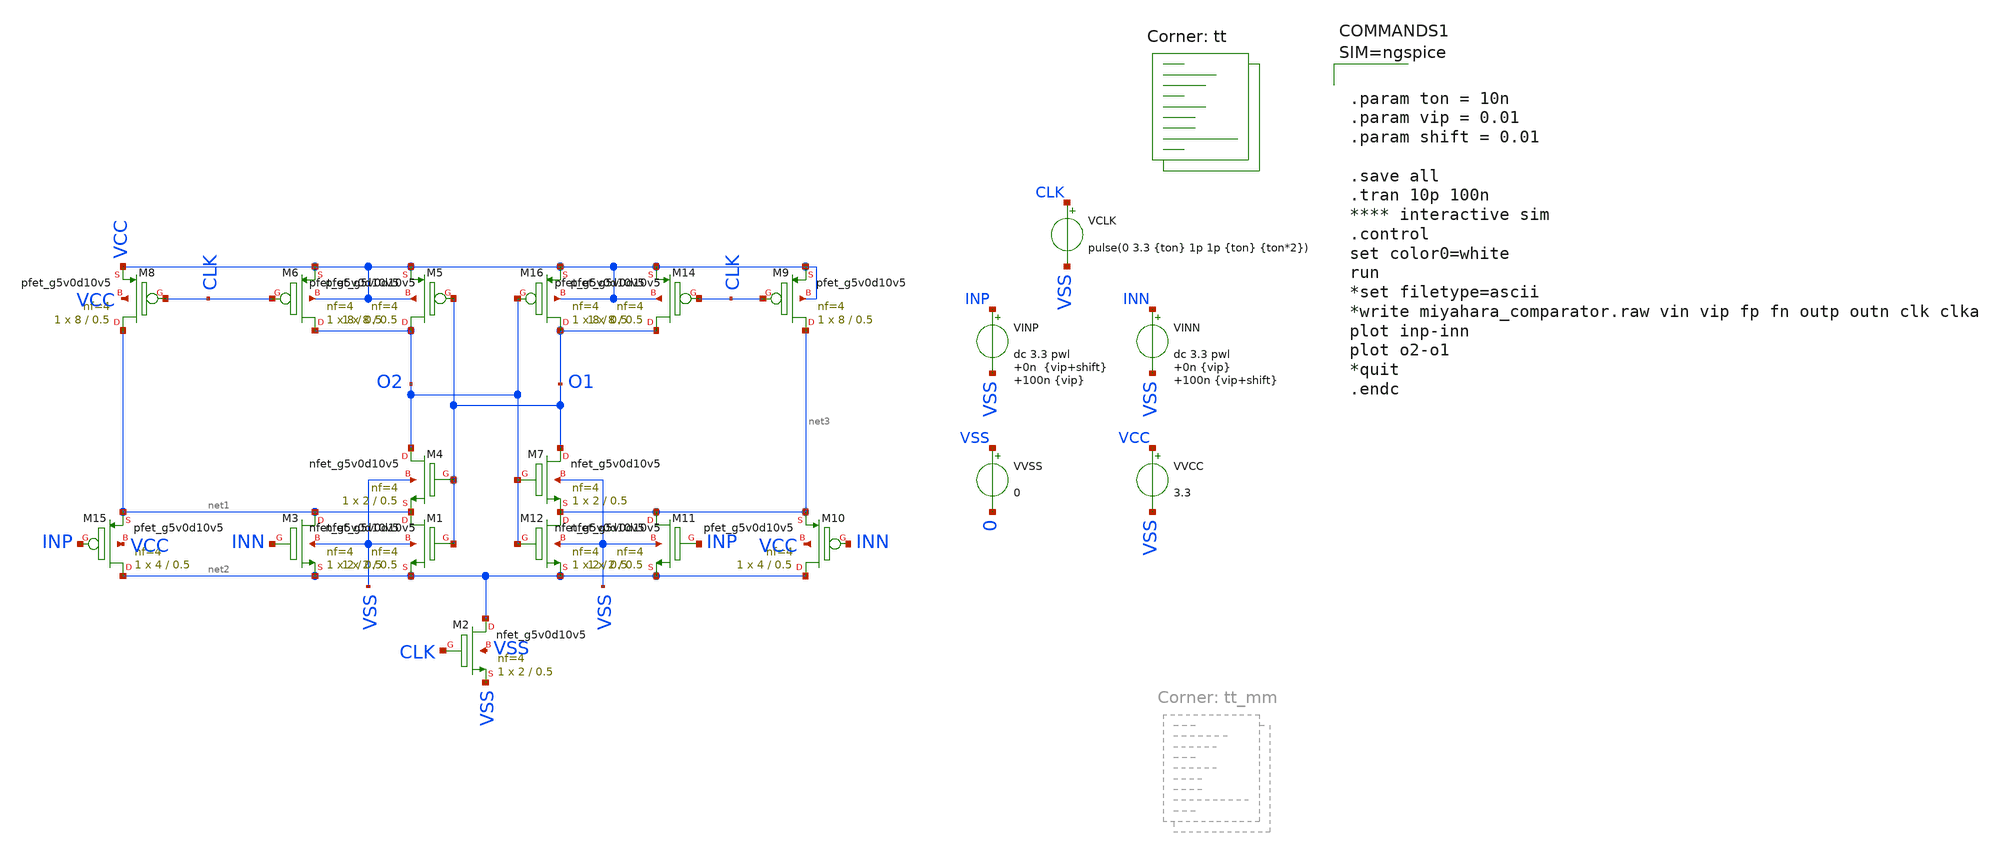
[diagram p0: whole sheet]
** sch_path: Comparator/schematic/new_comparator/comparator_rail2rail_working.sch
**.subckt comparator_rail2rail_working
VINP INP VSS dc 3.3 pwl 0n {vip+shift} 100n {vip}
VINN INN VSS dc 3.3 pwl 0n {vip} 100n {vip+shift}
XM15 net2 INP net1 VCC sky130_fd_pr__pfet_g5v0d10v5 L=0.5 W=4 nf=4 ad='int((nf+1)/2) * W/nf * 0.29' as='int((nf+2)/2) * W/nf * 0.29'
+ pd='2*int((nf+1)/2) * (W/nf + 0.29)' ps='2*int((nf+2)/2) * (W/nf + 0.29)' nrd='0.29 / W' nrs='0.29 / W'
+ sa=0 sb=0 sd=0 mult=1 m=1
XM2 net2 CLK VSS VSS sky130_fd_pr__nfet_g5v0d10v5 L=0.5 W=2 nf=4 ad='int((nf+1)/2) * W/nf * 0.29' as='int((nf+2)/2) * W/nf * 0.29'
+ pd='2*int((nf+1)/2) * (W/nf + 0.29)' ps='2*int((nf+2)/2) * (W/nf + 0.29)' nrd='0.29 / W' nrs='0.29 / W'
+ sa=0 sb=0 sd=0 mult=1 m=1
XM8 net1 CLK VCC VCC sky130_fd_pr__pfet_g5v0d10v5 L=0.5 W=8 nf=4 ad='int((nf+1)/2) * W/nf * 0.29' as='int((nf+2)/2) * W/nf * 0.29'
+ pd='2*int((nf+1)/2) * (W/nf + 0.29)' ps='2*int((nf+2)/2) * (W/nf + 0.29)' nrd='0.29 / W' nrs='0.29 / W'
+ sa=0 sb=0 sd=0 mult=1 m=1
XM1 net1 O1 net2 VSS sky130_fd_pr__nfet_g5v0d10v5 L=0.5 W=2 nf=4 ad='int((nf+1)/2) * W/nf * 0.29' as='int((nf+2)/2) * W/nf * 0.29'
+ pd='2*int((nf+1)/2) * (W/nf + 0.29)' ps='2*int((nf+2)/2) * (W/nf + 0.29)' nrd='0.29 / W' nrs='0.29 / W'
+ sa=0 sb=0 sd=0 mult=1 m=1
XM3 net1 INN net2 VSS sky130_fd_pr__nfet_g5v0d10v5 L=0.5 W=2 nf=4 ad='int((nf+1)/2) * W/nf * 0.29' as='int((nf+2)/2) * W/nf * 0.29'
+ pd='2*int((nf+1)/2) * (W/nf + 0.29)' ps='2*int((nf+2)/2) * (W/nf + 0.29)' nrd='0.29 / W' nrs='0.29 / W'
+ sa=0 sb=0 sd=0 mult=1 m=1
XM4 O2 O1 net1 VSS sky130_fd_pr__nfet_g5v0d10v5 L=0.5 W=2 nf=4 ad='int((nf+1)/2) * W/nf * 0.29' as='int((nf+2)/2) * W/nf * 0.29'
+ pd='2*int((nf+1)/2) * (W/nf + 0.29)' ps='2*int((nf+2)/2) * (W/nf + 0.29)' nrd='0.29 / W' nrs='0.29 / W'
+ sa=0 sb=0 sd=0 mult=1 m=1
XM5 O2 O1 VCC VCC sky130_fd_pr__pfet_g5v0d10v5 L=0.5 W=8 nf=4 ad='int((nf+1)/2) * W/nf * 0.29' as='int((nf+2)/2) * W/nf * 0.29'
+ pd='2*int((nf+1)/2) * (W/nf + 0.29)' ps='2*int((nf+2)/2) * (W/nf + 0.29)' nrd='0.29 / W' nrs='0.29 / W'
+ sa=0 sb=0 sd=0 mult=1 m=1
XM6 O2 CLK VCC VCC sky130_fd_pr__pfet_g5v0d10v5 L=0.5 W=8 nf=4 ad='int((nf+1)/2) * W/nf * 0.29' as='int((nf+2)/2) * W/nf * 0.29'
+ pd='2*int((nf+1)/2) * (W/nf + 0.29)' ps='2*int((nf+2)/2) * (W/nf + 0.29)' nrd='0.29 / W' nrs='0.29 / W'
+ sa=0 sb=0 sd=0 mult=1 m=1
XM11 net3 INP net2 VSS sky130_fd_pr__nfet_g5v0d10v5 L=0.5 W=2 nf=4 ad='int((nf+1)/2) * W/nf * 0.29' as='int((nf+2)/2) * W/nf * 0.29'
+ pd='2*int((nf+1)/2) * (W/nf + 0.29)' ps='2*int((nf+2)/2) * (W/nf + 0.29)' nrd='0.29 / W' nrs='0.29 / W'
+ sa=0 sb=0 sd=0 mult=1 m=1
XM12 net3 O2 net2 VSS sky130_fd_pr__nfet_g5v0d10v5 L=0.5 W=2 nf=4 ad='int((nf+1)/2) * W/nf * 0.29' as='int((nf+2)/2) * W/nf * 0.29'
+ pd='2*int((nf+1)/2) * (W/nf + 0.29)' ps='2*int((nf+2)/2) * (W/nf + 0.29)' nrd='0.29 / W' nrs='0.29 / W'
+ sa=0 sb=0 sd=0 mult=1 m=1
XM14 O1 CLK VCC VCC sky130_fd_pr__pfet_g5v0d10v5 L=0.5 W=8 nf=4 ad='int((nf+1)/2) * W/nf * 0.29' as='int((nf+2)/2) * W/nf * 0.29'
+ pd='2*int((nf+1)/2) * (W/nf + 0.29)' ps='2*int((nf+2)/2) * (W/nf + 0.29)' nrd='0.29 / W' nrs='0.29 / W'
+ sa=0 sb=0 sd=0 mult=1 m=1
XM16 O1 O2 VCC VCC sky130_fd_pr__pfet_g5v0d10v5 L=0.5 W=8 nf=4 ad='int((nf+1)/2) * W/nf * 0.29' as='int((nf+2)/2) * W/nf * 0.29'
+ pd='2*int((nf+1)/2) * (W/nf + 0.29)' ps='2*int((nf+2)/2) * (W/nf + 0.29)' nrd='0.29 / W' nrs='0.29 / W'
+ sa=0 sb=0 sd=0 mult=1 m=1
XM7 O1 O2 net3 VSS sky130_fd_pr__nfet_g5v0d10v5 L=0.5 W=2 nf=4 ad='int((nf+1)/2) * W/nf * 0.29' as='int((nf+2)/2) * W/nf * 0.29'
+ pd='2*int((nf+1)/2) * (W/nf + 0.29)' ps='2*int((nf+2)/2) * (W/nf + 0.29)' nrd='0.29 / W' nrs='0.29 / W'
+ sa=0 sb=0 sd=0 mult=1 m=1
XM9 net3 CLK VCC VCC sky130_fd_pr__pfet_g5v0d10v5 L=0.5 W=8 nf=4 ad='int((nf+1)/2) * W/nf * 0.29' as='int((nf+2)/2) * W/nf * 0.29'
+ pd='2*int((nf+1)/2) * (W/nf + 0.29)' ps='2*int((nf+2)/2) * (W/nf + 0.29)' nrd='0.29 / W' nrs='0.29 / W'
+ sa=0 sb=0 sd=0 mult=1 m=1
XM10 net2 INN net3 VCC sky130_fd_pr__pfet_g5v0d10v5 L=0.5 W=4 nf=4 ad='int((nf+1)/2) * W/nf * 0.29' as='int((nf+2)/2) * W/nf * 0.29'
+ pd='2*int((nf+1)/2) * (W/nf + 0.29)' ps='2*int((nf+2)/2) * (W/nf + 0.29)' nrd='0.29 / W' nrs='0.29 / W'
+ sa=0 sb=0 sd=0 mult=1 m=1
VVSS VSS 0 0
VVCC VCC VSS 3.3
VCLK CLK VSS pulse(0 3.3 {ton} 1p 1p {ton} {ton*2})
**** begin user architecture code
.lib $::SKYWATER_MODELS/sky130.lib.spice tt



.param ton = 10n
.param vip = 0.01
.param shift = 0.01

.save all
.tran 10p 100n
**** interactive sim
.control
set color0=white
run
*set filetype=ascii
*write miyahara_comparator.raw vin vip fp fn outp outn clk clka
plot inp-inn
plot o2-o1
*quit
.endc



**** end user architecture code
**.ends
.end
